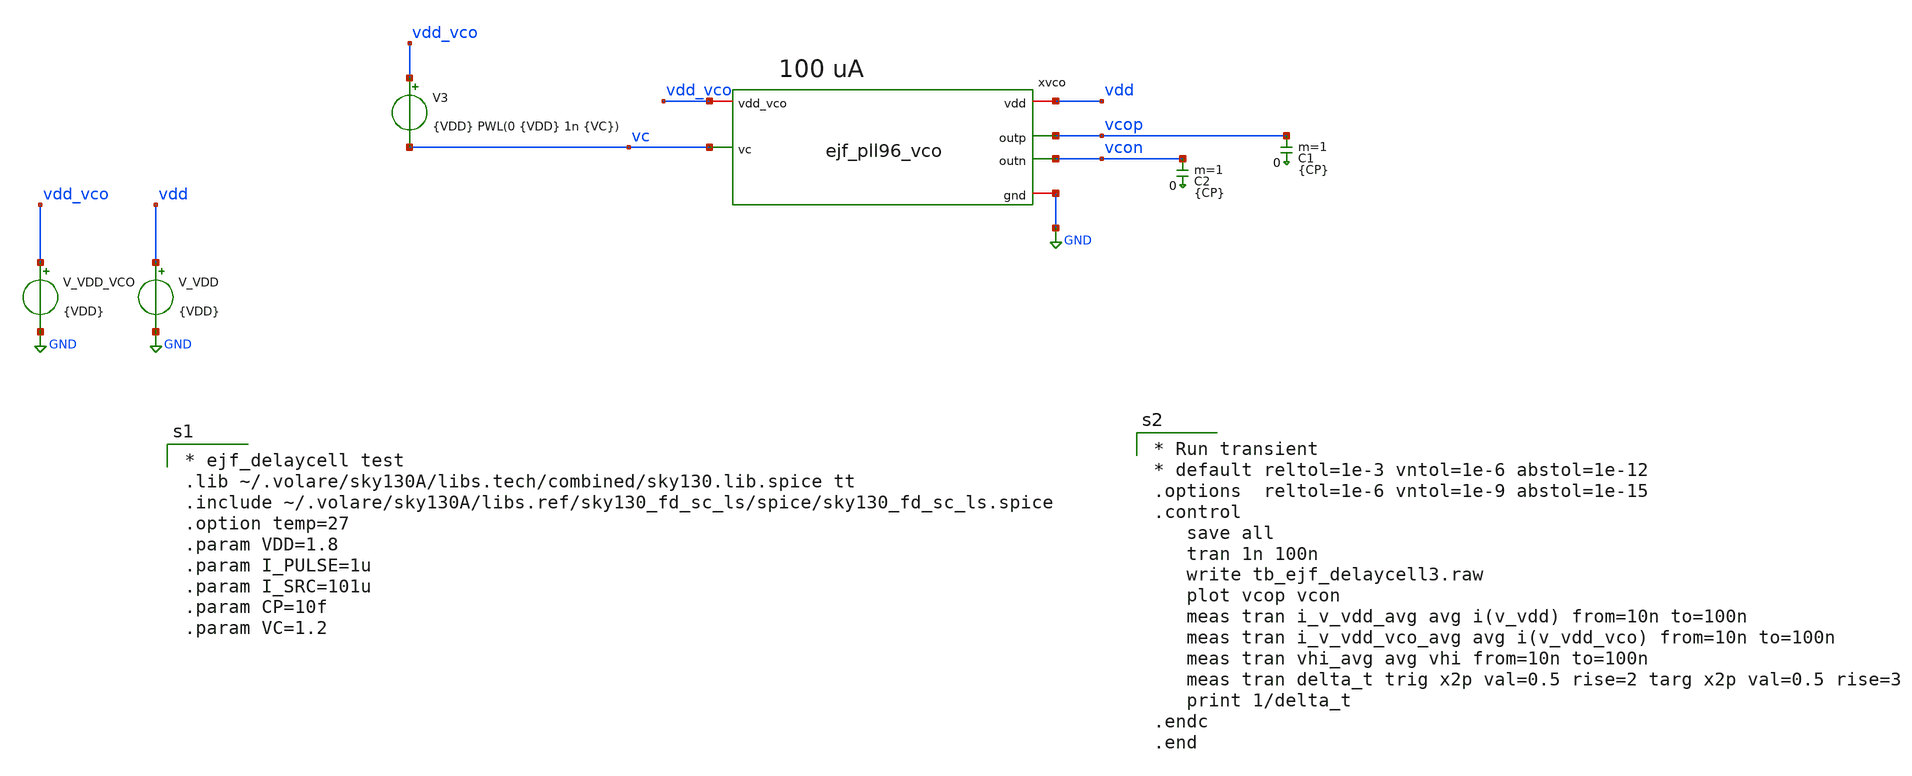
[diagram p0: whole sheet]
** sch_path: xschem/tb_ejf_pll96_vco.sch
**.subckt tb_ejf_pll96_vco
V_VDD vdd GND {VDD}
C1 vcop 0 {CP} m=1
C2 vcon 0 {CP} m=1
V3 vdd_vco vc {VDD} PWL(0 {VDD} 1n {VC})
xvco vdd_vco vc vdd vcop vcon GND ejf_pll96_vco
V_VDD_VCO vdd_vco GND {VDD}
**** begin user architecture code

* ejf_delaycell test
.lib ~/.volare/sky130A/libs.tech/combined/sky130.lib.spice tt
.include ~/.volare/sky130A/libs.ref/sky130_fd_sc_ls/spice/sky130_fd_sc_ls.spice
.option temp=27
.param VDD=1.8
.param I_PULSE=1u
.param I_SRC=101u
.param CP=10f
.param VC=1.2



* Run transient
* default reltol=1e-3 vntol=1e-6 abstol=1e-12
.options  reltol=1e-6 vntol=1e-9 abstol=1e-15
.control
   save all
   tran 1n 100n
   write tb_ejf_delaycell3.raw
   plot vcop vcon
   meas tran i_v_vdd_avg avg i(v_vdd) from=10n to=100n
   meas tran i_v_vdd_vco_avg avg i(v_vdd_vco) from=10n to=100n
   meas tran vhi_avg avg vhi from=10n to=100n
   meas tran delta_t trig x2p val=0.5 rise=2 targ x2p val=0.5 rise=3
   print 1/delta_t
.endc
.end

**** end user architecture code
**.ends
.GLOBAL GND
.end
